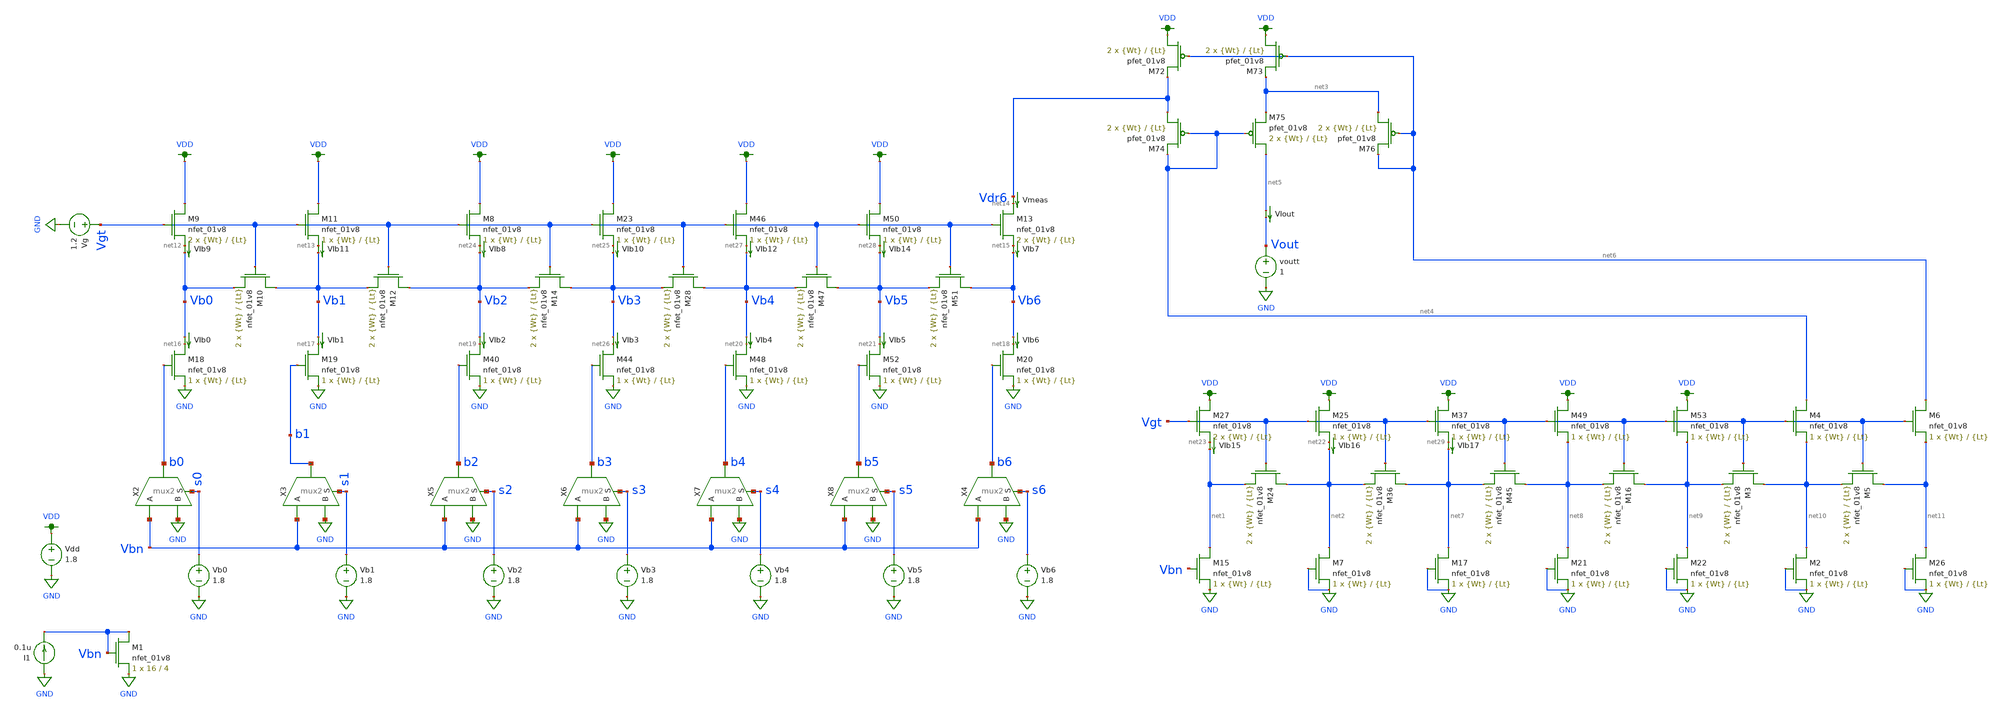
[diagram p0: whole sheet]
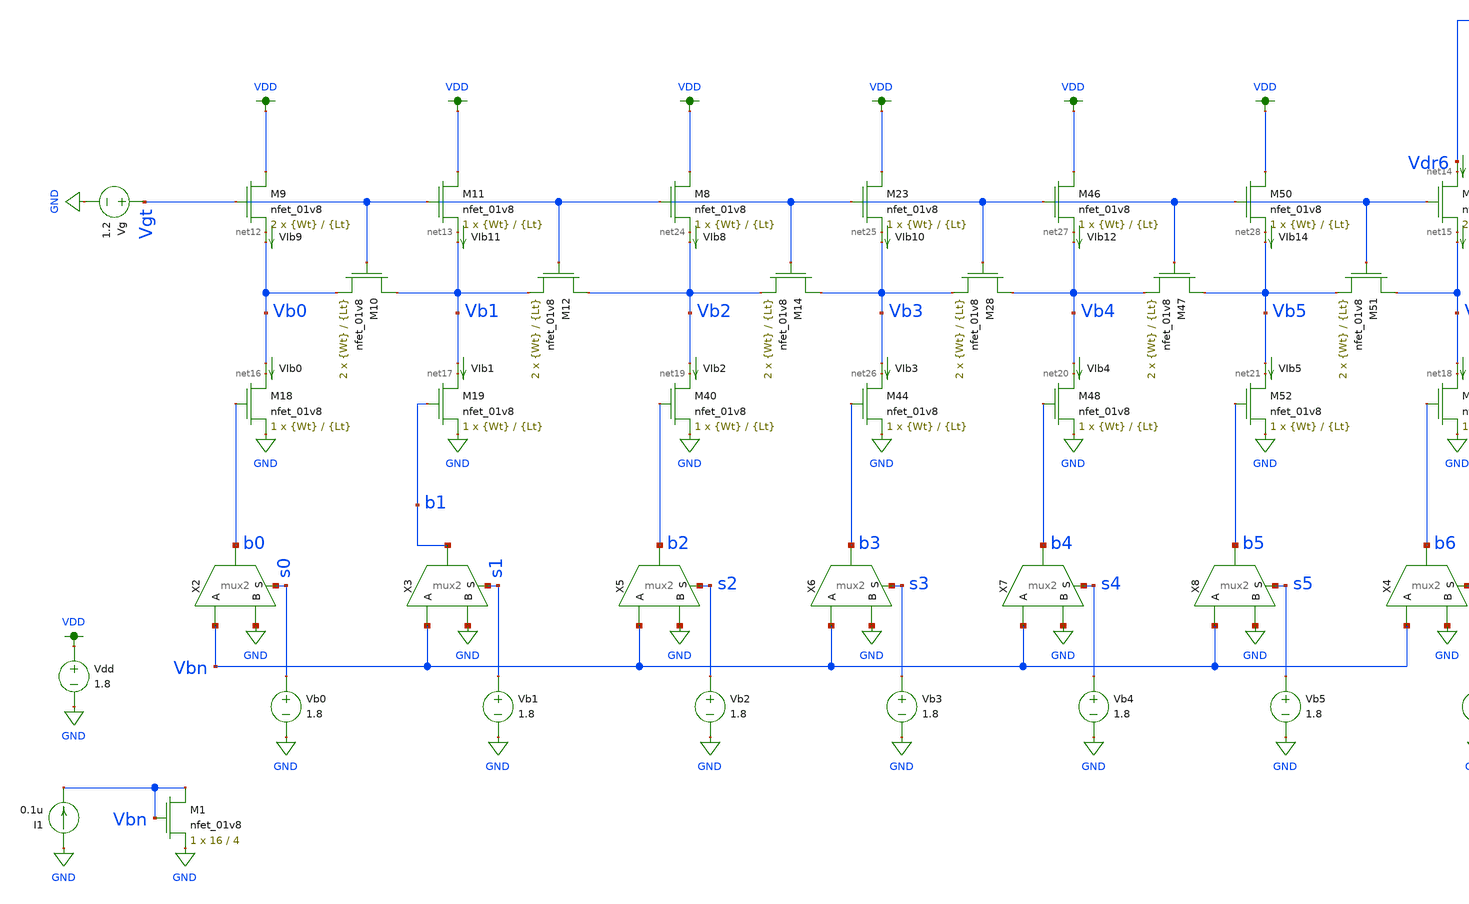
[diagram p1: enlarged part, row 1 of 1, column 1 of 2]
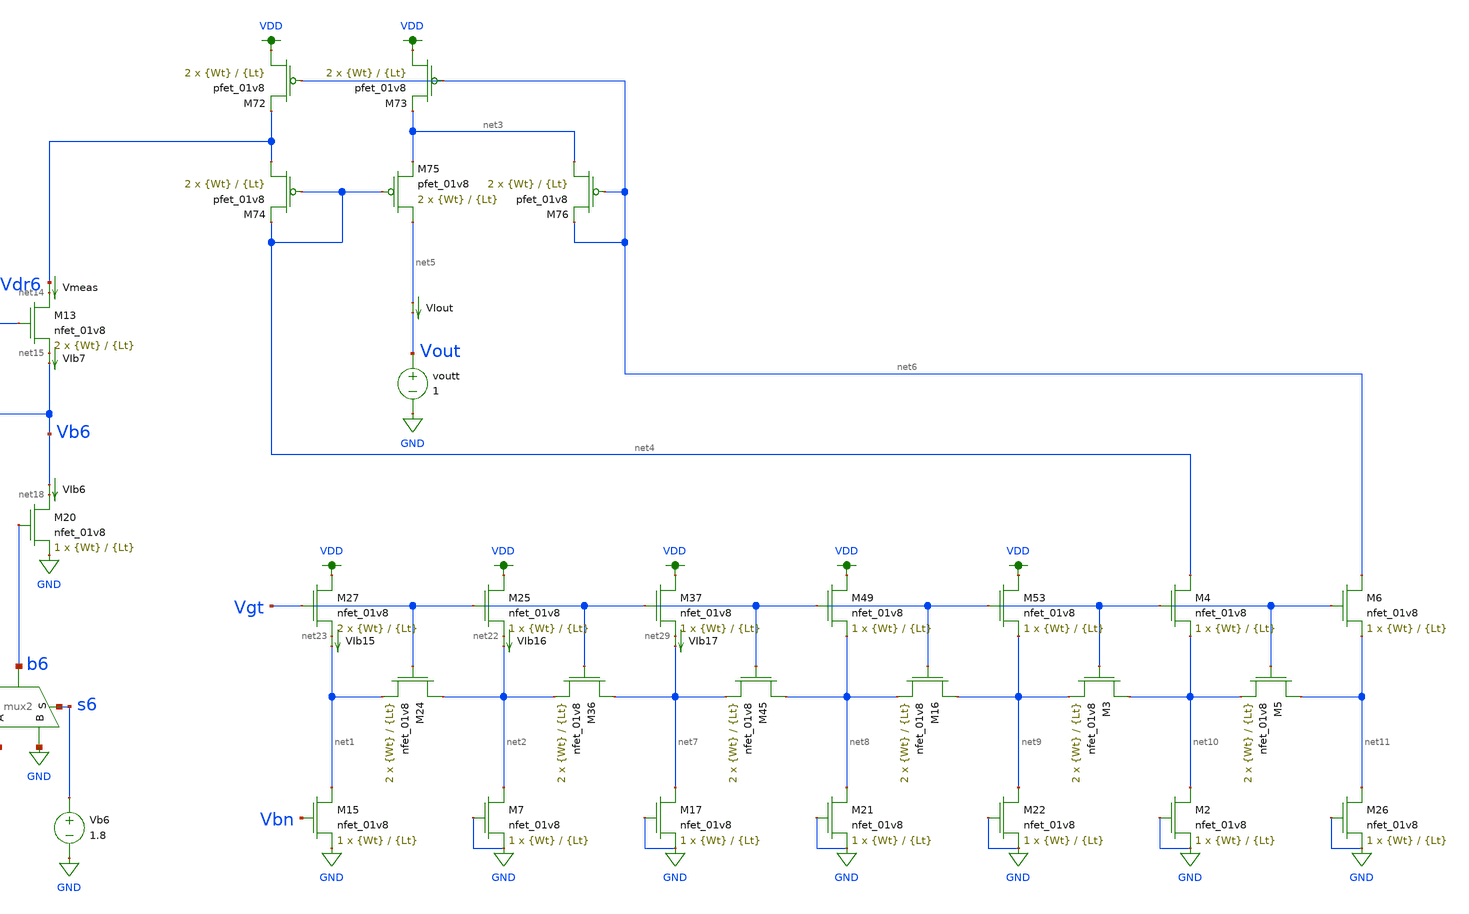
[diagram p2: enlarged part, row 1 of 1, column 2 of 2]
** sch_path: schematic/LDS/test/ladder_ogtest.sch
**.subckt ladder_ogtest
X2 b0 Vbn GND s0 mux2
X3 b1 Vbn GND s1 mux2
Vdd VDD GND 1.8
Vb0 s0 GND 1.8
Vb1 s1 GND 1.8
Vb2 s2 GND 1.8
XM9 VDD Vgt net12 GND sky130_fd_pr__nfet_01v8 L={Lt} W={Wt} nf=1 ad='int((nf+1)/2) * W/nf * 0.29' as='int((nf+2)/2) * W/nf * 0.29'
+ pd='2*int((nf+1)/2) * (W/nf + 0.29)' ps='2*int((nf+2)/2) * (W/nf + 0.29)' nrd='0.29 / W' nrs='0.29 / W'
+ sa=0 sb=0 sd=0 mult=2 m=2
XM10 Vb1 Vgt Vb0 GND sky130_fd_pr__nfet_01v8 L={Lt} W={Wt} nf=1 ad='int((nf+1)/2) * W/nf * 0.29' as='int((nf+2)/2) * W/nf * 0.29'
+ pd='2*int((nf+1)/2) * (W/nf + 0.29)' ps='2*int((nf+2)/2) * (W/nf + 0.29)' nrd='0.29 / W' nrs='0.29 / W'
+ sa=0 sb=0 sd=0 mult=2 m=2
XM11 VDD Vgt net13 GND sky130_fd_pr__nfet_01v8 L={Lt} W={Wt} nf=1 ad='int((nf+1)/2) * W/nf * 0.29' as='int((nf+2)/2) * W/nf * 0.29'
+ pd='2*int((nf+1)/2) * (W/nf + 0.29)' ps='2*int((nf+2)/2) * (W/nf + 0.29)' nrd='0.29 / W' nrs='0.29 / W'
+ sa=0 sb=0 sd=0 mult=1 m=1
XM12 Vb2 Vgt Vb1 GND sky130_fd_pr__nfet_01v8 L={Lt} W={Wt} nf=1 ad='int((nf+1)/2) * W/nf * 0.29' as='int((nf+2)/2) * W/nf * 0.29'
+ pd='2*int((nf+1)/2) * (W/nf + 0.29)' ps='2*int((nf+2)/2) * (W/nf + 0.29)' nrd='0.29 / W' nrs='0.29 / W'
+ sa=0 sb=0 sd=0 mult=2 m=2
XM13 net14 Vgt net15 GND sky130_fd_pr__nfet_01v8 L={Lt} W={Wt} nf=1 ad='int((nf+1)/2) * W/nf * 0.29'
+ as='int((nf+2)/2) * W/nf * 0.29' pd='2*int((nf+1)/2) * (W/nf + 0.29)' ps='2*int((nf+2)/2) * (W/nf + 0.29)'
+ nrd='0.29 / W' nrs='0.29 / W' sa=0 sb=0 sd=0 mult=2 m=2
XM18 net16 b0 GND GND sky130_fd_pr__nfet_01v8 L={Lt} W={Wt} nf=1 ad='int((nf+1)/2) * W/nf * 0.29' as='int((nf+2)/2) * W/nf * 0.29'
+ pd='2*int((nf+1)/2) * (W/nf + 0.29)' ps='2*int((nf+2)/2) * (W/nf + 0.29)' nrd='0.29 / W' nrs='0.29 / W'
+ sa=0 sb=0 sd=0 mult=1 m=1
XM19 net17 b1 GND GND sky130_fd_pr__nfet_01v8 L={Lt} W={Wt} nf=1 ad='int((nf+1)/2) * W/nf * 0.29' as='int((nf+2)/2) * W/nf * 0.29'
+ pd='2*int((nf+1)/2) * (W/nf + 0.29)' ps='2*int((nf+2)/2) * (W/nf + 0.29)' nrd='0.29 / W' nrs='0.29 / W'
+ sa=0 sb=0 sd=0 mult=1 m=1
XM20 net18 b6 GND GND sky130_fd_pr__nfet_01v8 L={Lt} W={Wt} nf=1 ad='int((nf+1)/2) * W/nf * 0.29' as='int((nf+2)/2) * W/nf * 0.29'
+ pd='2*int((nf+1)/2) * (W/nf + 0.29)' ps='2*int((nf+2)/2) * (W/nf + 0.29)' nrd='0.29 / W' nrs='0.29 / W'
+ sa=0 sb=0 sd=0 mult=1 m=1
Vmeas Vdr6 net14 0
.save i(vmeas)
VIb0 Vb0 net16 0
.save i(vib0)
VIb1 Vb1 net17 0
.save i(vib1)
VIb2 Vb2 net19 0
.save i(vib2)
VIb4 Vb4 net20 0
.save i(vib4)
VIb5 Vb5 net21 0
.save i(vib5)
VIb6 Vb6 net18 0
.save i(vib6)
VIout net5 Vout 0
.save i(viout)
XM24 net2 Vgt net1 GND sky130_fd_pr__nfet_01v8 L={Lt} W={Wt} nf=1 ad='int((nf+1)/2) * W/nf * 0.29' as='int((nf+2)/2) * W/nf * 0.29'
+ pd='2*int((nf+1)/2) * (W/nf + 0.29)' ps='2*int((nf+2)/2) * (W/nf + 0.29)' nrd='0.29 / W' nrs='0.29 / W'
+ sa=0 sb=0 sd=0 mult=2 m=2
XM25 VDD Vgt net22 GND sky130_fd_pr__nfet_01v8 L={Lt} W={Wt} nf=1 ad='int((nf+1)/2) * W/nf * 0.29' as='int((nf+2)/2) * W/nf * 0.29'
+ pd='2*int((nf+1)/2) * (W/nf + 0.29)' ps='2*int((nf+2)/2) * (W/nf + 0.29)' nrd='0.29 / W' nrs='0.29 / W'
+ sa=0 sb=0 sd=0 mult=1 m=1
XM27 VDD Vgt net23 GND sky130_fd_pr__nfet_01v8 L={Lt} W={Wt} nf=1 ad='int((nf+1)/2) * W/nf * 0.29' as='int((nf+2)/2) * W/nf * 0.29'
+ pd='2*int((nf+1)/2) * (W/nf + 0.29)' ps='2*int((nf+2)/2) * (W/nf + 0.29)' nrd='0.29 / W' nrs='0.29 / W'
+ sa=0 sb=0 sd=0 mult=2 m=2
XM72 VDD net6 Vdr6 VDD sky130_fd_pr__pfet_01v8 L={Lt} W={Wt} nf=1 ad='int((nf+1)/2) * W/nf * 0.29' as='int((nf+2)/2) * W/nf * 0.29'
+ pd='2*int((nf+1)/2) * (W/nf + 0.29)' ps='2*int((nf+2)/2) * (W/nf + 0.29)' nrd='0.29 / W' nrs='0.29 / W'
+ sa=0 sb=0 sd=0 mult=2 m=2
XM73 VDD net6 net3 VDD sky130_fd_pr__pfet_01v8 L={Lt} W={Wt} nf=1 ad='int((nf+1)/2) * W/nf * 0.29' as='int((nf+2)/2) * W/nf * 0.29'
+ pd='2*int((nf+1)/2) * (W/nf + 0.29)' ps='2*int((nf+2)/2) * (W/nf + 0.29)' nrd='0.29 / W' nrs='0.29 / W'
+ sa=0 sb=0 sd=0 mult=2 m=2
XM74 Vdr6 net4 net4 VDD sky130_fd_pr__pfet_01v8 L={Lt} W={Wt} nf=1 ad='int((nf+1)/2) * W/nf * 0.29' as='int((nf+2)/2) * W/nf * 0.29'
+ pd='2*int((nf+1)/2) * (W/nf + 0.29)' ps='2*int((nf+2)/2) * (W/nf + 0.29)' nrd='0.29 / W' nrs='0.29 / W'
+ sa=0 sb=0 sd=0 mult=2 m=2
XM75 net5 net4 net3 VDD sky130_fd_pr__pfet_01v8 L={Lt} W={Wt} nf=1 ad='int((nf+1)/2) * W/nf * 0.29' as='int((nf+2)/2) * W/nf * 0.29'
+ pd='2*int((nf+1)/2) * (W/nf + 0.29)' ps='2*int((nf+2)/2) * (W/nf + 0.29)' nrd='0.29 / W' nrs='0.29 / W'
+ sa=0 sb=0 sd=0 mult=2 m=2
XM76 net3 net6 net6 VDD sky130_fd_pr__pfet_01v8 L={Lt} W={Wt} nf=1 ad='int((nf+1)/2) * W/nf * 0.29' as='int((nf+2)/2) * W/nf * 0.29'
+ pd='2*int((nf+1)/2) * (W/nf + 0.29)' ps='2*int((nf+2)/2) * (W/nf + 0.29)' nrd='0.29 / W' nrs='0.29 / W'
+ sa=0 sb=0 sd=0 mult=2 m=2
X5 b2 Vbn GND s2 mux2
Vb3 s3 GND 1.8
XM8 VDD Vgt net24 GND sky130_fd_pr__nfet_01v8 L={Lt} W={Wt} nf=1 ad='int((nf+1)/2) * W/nf * 0.29' as='int((nf+2)/2) * W/nf * 0.29'
+ pd='2*int((nf+1)/2) * (W/nf + 0.29)' ps='2*int((nf+2)/2) * (W/nf + 0.29)' nrd='0.29 / W' nrs='0.29 / W'
+ sa=0 sb=0 sd=0 mult=1 m=1
XM14 Vb3 Vgt Vb2 GND sky130_fd_pr__nfet_01v8 L={Lt} W={Wt} nf=1 ad='int((nf+1)/2) * W/nf * 0.29' as='int((nf+2)/2) * W/nf * 0.29'
+ pd='2*int((nf+1)/2) * (W/nf + 0.29)' ps='2*int((nf+2)/2) * (W/nf + 0.29)' nrd='0.29 / W' nrs='0.29 / W'
+ sa=0 sb=0 sd=0 mult=2 m=2
XM40 net19 b2 GND GND sky130_fd_pr__nfet_01v8 L={Lt} W={Wt} nf=1 ad='int((nf+1)/2) * W/nf * 0.29' as='int((nf+2)/2) * W/nf * 0.29'
+ pd='2*int((nf+1)/2) * (W/nf + 0.29)' ps='2*int((nf+2)/2) * (W/nf + 0.29)' nrd='0.29 / W' nrs='0.29 / W'
+ sa=0 sb=0 sd=0 mult=1 m=1
VIb7 net15 Vb6 0
.save i(vib7)
VIb8 net24 Vb2 0
.save i(vib8)
X6 b3 Vbn GND s3 mux2
Vb4 s4 GND 1.8
XM23 VDD Vgt net25 GND sky130_fd_pr__nfet_01v8 L={Lt} W={Wt} nf=1 ad='int((nf+1)/2) * W/nf * 0.29' as='int((nf+2)/2) * W/nf * 0.29'
+ pd='2*int((nf+1)/2) * (W/nf + 0.29)' ps='2*int((nf+2)/2) * (W/nf + 0.29)' nrd='0.29 / W' nrs='0.29 / W'
+ sa=0 sb=0 sd=0 mult=1 m=1
XM28 Vb4 Vgt Vb3 GND sky130_fd_pr__nfet_01v8 L={Lt} W={Wt} nf=1 ad='int((nf+1)/2) * W/nf * 0.29' as='int((nf+2)/2) * W/nf * 0.29'
+ pd='2*int((nf+1)/2) * (W/nf + 0.29)' ps='2*int((nf+2)/2) * (W/nf + 0.29)' nrd='0.29 / W' nrs='0.29 / W'
+ sa=0 sb=0 sd=0 mult=2 m=2
XM44 net26 b3 GND GND sky130_fd_pr__nfet_01v8 L={Lt} W={Wt} nf=1 ad='int((nf+1)/2) * W/nf * 0.29' as='int((nf+2)/2) * W/nf * 0.29'
+ pd='2*int((nf+1)/2) * (W/nf + 0.29)' ps='2*int((nf+2)/2) * (W/nf + 0.29)' nrd='0.29 / W' nrs='0.29 / W'
+ sa=0 sb=0 sd=0 mult=1 m=1
VIb3 Vb3 net26 0
.save i(vib3)
VIb10 net25 Vb3 0
.save i(vib10)
X7 b4 Vbn GND s4 mux2
Vb5 s5 GND 1.8
XM46 VDD Vgt net27 GND sky130_fd_pr__nfet_01v8 L={Lt} W={Wt} nf=1 ad='int((nf+1)/2) * W/nf * 0.29' as='int((nf+2)/2) * W/nf * 0.29'
+ pd='2*int((nf+1)/2) * (W/nf + 0.29)' ps='2*int((nf+2)/2) * (W/nf + 0.29)' nrd='0.29 / W' nrs='0.29 / W'
+ sa=0 sb=0 sd=0 mult=1 m=1
XM47 Vb5 Vgt Vb4 GND sky130_fd_pr__nfet_01v8 L={Lt} W={Wt} nf=1 ad='int((nf+1)/2) * W/nf * 0.29' as='int((nf+2)/2) * W/nf * 0.29'
+ pd='2*int((nf+1)/2) * (W/nf + 0.29)' ps='2*int((nf+2)/2) * (W/nf + 0.29)' nrd='0.29 / W' nrs='0.29 / W'
+ sa=0 sb=0 sd=0 mult=2 m=2
XM48 net20 b4 GND GND sky130_fd_pr__nfet_01v8 L={Lt} W={Wt} nf=1 ad='int((nf+1)/2) * W/nf * 0.29' as='int((nf+2)/2) * W/nf * 0.29'
+ pd='2*int((nf+1)/2) * (W/nf + 0.29)' ps='2*int((nf+2)/2) * (W/nf + 0.29)' nrd='0.29 / W' nrs='0.29 / W'
+ sa=0 sb=0 sd=0 mult=1 m=1
VIb9 net12 Vb0 0
.save i(vib9)
VIb12 net27 Vb4 0
.save i(vib12)
X8 b5 Vbn GND s5 mux2
XM50 VDD Vgt net28 GND sky130_fd_pr__nfet_01v8 L={Lt} W={Wt} nf=1 ad='int((nf+1)/2) * W/nf * 0.29' as='int((nf+2)/2) * W/nf * 0.29'
+ pd='2*int((nf+1)/2) * (W/nf + 0.29)' ps='2*int((nf+2)/2) * (W/nf + 0.29)' nrd='0.29 / W' nrs='0.29 / W'
+ sa=0 sb=0 sd=0 mult=1 m=1
XM51 Vb6 Vgt Vb5 GND sky130_fd_pr__nfet_01v8 L={Lt} W={Wt} nf=1 ad='int((nf+1)/2) * W/nf * 0.29' as='int((nf+2)/2) * W/nf * 0.29'
+ pd='2*int((nf+1)/2) * (W/nf + 0.29)' ps='2*int((nf+2)/2) * (W/nf + 0.29)' nrd='0.29 / W' nrs='0.29 / W'
+ sa=0 sb=0 sd=0 mult=2 m=2
XM52 net21 b5 GND GND sky130_fd_pr__nfet_01v8 L={Lt} W={Wt} nf=1 ad='int((nf+1)/2) * W/nf * 0.29' as='int((nf+2)/2) * W/nf * 0.29'
+ pd='2*int((nf+1)/2) * (W/nf + 0.29)' ps='2*int((nf+2)/2) * (W/nf + 0.29)' nrd='0.29 / W' nrs='0.29 / W'
+ sa=0 sb=0 sd=0 mult=1 m=1
VIb11 net13 Vb1 0
.save i(vib11)
VIb14 net28 Vb5 0
.save i(vib14)
Vb6 s6 GND 1.8
X4 b6 Vbn GND s6 mux2
XM15 net1 Vbn GND GND sky130_fd_pr__nfet_01v8 L={Lt} W={Wt} nf=1 ad='int((nf+1)/2) * W/nf * 0.29' as='int((nf+2)/2) * W/nf * 0.29'
+ pd='2*int((nf+1)/2) * (W/nf + 0.29)' ps='2*int((nf+2)/2) * (W/nf + 0.29)' nrd='0.29 / W' nrs='0.29 / W'
+ sa=0 sb=0 sd=0 mult=1 m=1
XM36 net7 Vgt net2 GND sky130_fd_pr__nfet_01v8 L={Lt} W={Wt} nf=1 ad='int((nf+1)/2) * W/nf * 0.29' as='int((nf+2)/2) * W/nf * 0.29'
+ pd='2*int((nf+1)/2) * (W/nf + 0.29)' ps='2*int((nf+2)/2) * (W/nf + 0.29)' nrd='0.29 / W' nrs='0.29 / W'
+ sa=0 sb=0 sd=0 mult=2 m=2
XM37 VDD Vgt net29 GND sky130_fd_pr__nfet_01v8 L={Lt} W={Wt} nf=1 ad='int((nf+1)/2) * W/nf * 0.29' as='int((nf+2)/2) * W/nf * 0.29'
+ pd='2*int((nf+1)/2) * (W/nf + 0.29)' ps='2*int((nf+2)/2) * (W/nf + 0.29)' nrd='0.29 / W' nrs='0.29 / W'
+ sa=0 sb=0 sd=0 mult=1 m=1
VIb15 net23 net1 0
.save i(vib15)
VIb16 net22 net2 0
.save i(vib16)
VIb17 net29 net7 0
.save i(vib17)
XM45 net8 Vgt net7 GND sky130_fd_pr__nfet_01v8 L={Lt} W={Wt} nf=1 ad='int((nf+1)/2) * W/nf * 0.29' as='int((nf+2)/2) * W/nf * 0.29'
+ pd='2*int((nf+1)/2) * (W/nf + 0.29)' ps='2*int((nf+2)/2) * (W/nf + 0.29)' nrd='0.29 / W' nrs='0.29 / W'
+ sa=0 sb=0 sd=0 mult=2 m=2
XM49 VDD Vgt net8 GND sky130_fd_pr__nfet_01v8 L={Lt} W={Wt} nf=1 ad='int((nf+1)/2) * W/nf * 0.29' as='int((nf+2)/2) * W/nf * 0.29'
+ pd='2*int((nf+1)/2) * (W/nf + 0.29)' ps='2*int((nf+2)/2) * (W/nf + 0.29)' nrd='0.29 / W' nrs='0.29 / W'
+ sa=0 sb=0 sd=0 mult=1 m=1
voutt Vout GND 1
XM16 net9 Vgt net8 GND sky130_fd_pr__nfet_01v8 L={Lt} W={Wt} nf=1 ad='int((nf+1)/2) * W/nf * 0.29' as='int((nf+2)/2) * W/nf * 0.29'
+ pd='2*int((nf+1)/2) * (W/nf + 0.29)' ps='2*int((nf+2)/2) * (W/nf + 0.29)' nrd='0.29 / W' nrs='0.29 / W'
+ sa=0 sb=0 sd=0 mult=2 m=2
XM53 VDD Vgt net9 GND sky130_fd_pr__nfet_01v8 L={Lt} W={Wt} nf=1 ad='int((nf+1)/2) * W/nf * 0.29' as='int((nf+2)/2) * W/nf * 0.29'
+ pd='2*int((nf+1)/2) * (W/nf + 0.29)' ps='2*int((nf+2)/2) * (W/nf + 0.29)' nrd='0.29 / W' nrs='0.29 / W'
+ sa=0 sb=0 sd=0 mult=1 m=1
XM3 net10 Vgt net9 GND sky130_fd_pr__nfet_01v8 L={Lt} W={Wt} nf=1 ad='int((nf+1)/2) * W/nf * 0.29' as='int((nf+2)/2) * W/nf * 0.29'
+ pd='2*int((nf+1)/2) * (W/nf + 0.29)' ps='2*int((nf+2)/2) * (W/nf + 0.29)' nrd='0.29 / W' nrs='0.29 / W'
+ sa=0 sb=0 sd=0 mult=2 m=2
XM4 net4 Vgt net10 GND sky130_fd_pr__nfet_01v8 L={Lt} W={Wt} nf=1 ad='int((nf+1)/2) * W/nf * 0.29' as='int((nf+2)/2) * W/nf * 0.29'
+ pd='2*int((nf+1)/2) * (W/nf + 0.29)' ps='2*int((nf+2)/2) * (W/nf + 0.29)' nrd='0.29 / W' nrs='0.29 / W'
+ sa=0 sb=0 sd=0 mult=1 m=1
XM5 net11 Vgt net10 GND sky130_fd_pr__nfet_01v8 L={Lt} W={Wt} nf=1 ad='int((nf+1)/2) * W/nf * 0.29' as='int((nf+2)/2) * W/nf * 0.29'
+ pd='2*int((nf+1)/2) * (W/nf + 0.29)' ps='2*int((nf+2)/2) * (W/nf + 0.29)' nrd='0.29 / W' nrs='0.29 / W'
+ sa=0 sb=0 sd=0 mult=2 m=2
XM6 net6 Vgt net11 GND sky130_fd_pr__nfet_01v8 L={Lt} W={Wt} nf=1 ad='int((nf+1)/2) * W/nf * 0.29' as='int((nf+2)/2) * W/nf * 0.29'
+ pd='2*int((nf+1)/2) * (W/nf + 0.29)' ps='2*int((nf+2)/2) * (W/nf + 0.29)' nrd='0.29 / W' nrs='0.29 / W'
+ sa=0 sb=0 sd=0 mult=1 m=1
Vg Vgt GND 1.2
I1 GND Vbn 0.1u
XM1 Vbn Vbn GND GND sky130_fd_pr__nfet_01v8 L=4 W=16 nf=1 ad='int((nf+1)/2) * W/nf * 0.29' as='int((nf+2)/2) * W/nf * 0.29'
+ pd='2*int((nf+1)/2) * (W/nf + 0.29)' ps='2*int((nf+2)/2) * (W/nf + 0.29)' nrd='0.29 / W' nrs='0.29 / W'
+ sa=0 sb=0 sd=0 mult=1 m=1
XM2 net10 GND GND GND sky130_fd_pr__nfet_01v8 L={Lt} W={Wt} nf=1 ad='int((nf+1)/2) * W/nf * 0.29' as='int((nf+2)/2) * W/nf * 0.29'
+ pd='2*int((nf+1)/2) * (W/nf + 0.29)' ps='2*int((nf+2)/2) * (W/nf + 0.29)' nrd='0.29 / W' nrs='0.29 / W'
+ sa=0 sb=0 sd=0 mult=1 m=1
XM7 net2 GND GND GND sky130_fd_pr__nfet_01v8 L={Lt} W={Wt} nf=1 ad='int((nf+1)/2) * W/nf * 0.29' as='int((nf+2)/2) * W/nf * 0.29'
+ pd='2*int((nf+1)/2) * (W/nf + 0.29)' ps='2*int((nf+2)/2) * (W/nf + 0.29)' nrd='0.29 / W' nrs='0.29 / W'
+ sa=0 sb=0 sd=0 mult=1 m=1
XM17 net7 GND GND GND sky130_fd_pr__nfet_01v8 L={Lt} W={Wt} nf=1 ad='int((nf+1)/2) * W/nf * 0.29' as='int((nf+2)/2) * W/nf * 0.29'
+ pd='2*int((nf+1)/2) * (W/nf + 0.29)' ps='2*int((nf+2)/2) * (W/nf + 0.29)' nrd='0.29 / W' nrs='0.29 / W'
+ sa=0 sb=0 sd=0 mult=1 m=1
XM21 net8 GND GND GND sky130_fd_pr__nfet_01v8 L={Lt} W={Wt} nf=1 ad='int((nf+1)/2) * W/nf * 0.29' as='int((nf+2)/2) * W/nf * 0.29'
+ pd='2*int((nf+1)/2) * (W/nf + 0.29)' ps='2*int((nf+2)/2) * (W/nf + 0.29)' nrd='0.29 / W' nrs='0.29 / W'
+ sa=0 sb=0 sd=0 mult=1 m=1
XM22 net9 GND GND GND sky130_fd_pr__nfet_01v8 L={Lt} W={Wt} nf=1 ad='int((nf+1)/2) * W/nf * 0.29' as='int((nf+2)/2) * W/nf * 0.29'
+ pd='2*int((nf+1)/2) * (W/nf + 0.29)' ps='2*int((nf+2)/2) * (W/nf + 0.29)' nrd='0.29 / W' nrs='0.29 / W'
+ sa=0 sb=0 sd=0 mult=1 m=1
XM26 net11 GND GND GND sky130_fd_pr__nfet_01v8 L={Lt} W={Wt} nf=1 ad='int((nf+1)/2) * W/nf * 0.29' as='int((nf+2)/2) * W/nf * 0.29'
+ pd='2*int((nf+1)/2) * (W/nf + 0.29)' ps='2*int((nf+2)/2) * (W/nf + 0.29)' nrd='0.29 / W' nrs='0.29 / W'
+ sa=0 sb=0 sd=0 mult=1 m=1
**** begin user architecture code

.option wnflag=1
.param MC_SWITCH=0.0
.lib ~/skywater/skywater-pdk/libraries/sky130_fd_pr_ngspice/latest/models/sky130.lib.spice tt


.param Wt = 16
.param Lt = 4
.control
tran 0.000001 10u 0.0001u
save all
plot i(viout) i(vmeas)
.endc

**** end user architecture code
**.ends
.GLOBAL GND
.GLOBAL VDD
.end
